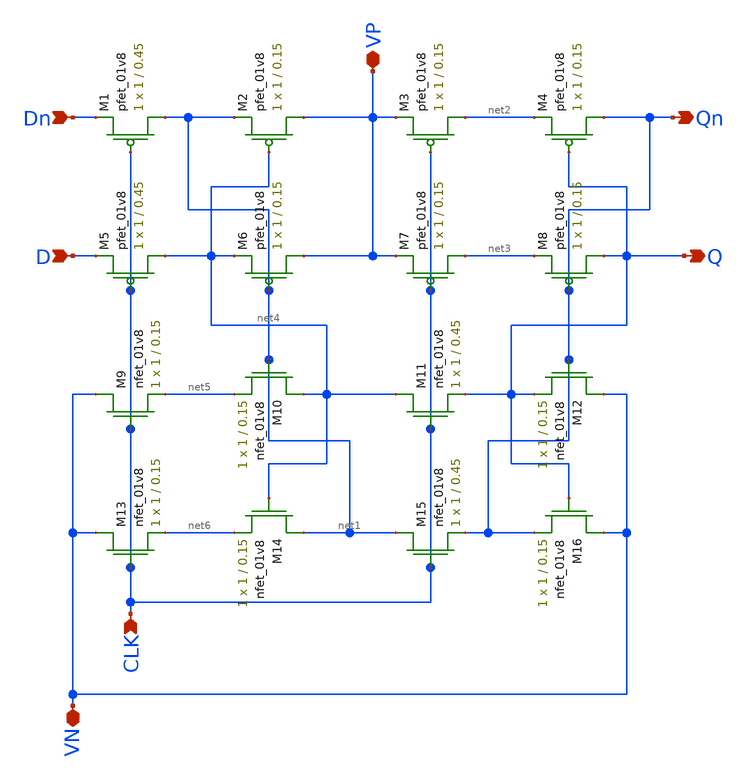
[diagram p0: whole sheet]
** sch_path: mp2/d_ff.sch
**.subckt d_ff D Dn CLK VN VP Qn Q
*.ipin D
*.ipin Dn
*.ipin CLK
*.iopin VN
*.iopin VP
*.opin Qn
*.opin Q
XM1 net1 CLK Dn VDD sky130_fd_pr__pfet_01v8 L=0.45 W=1 nf=1 ad='int((nf+1)/2) * W/nf * 0.29' as='int((nf+2)/2) * W/nf * 0.29'
+ pd='2*int((nf+1)/2) * (W/nf + 0.29)' ps='2*int((nf+2)/2) * (W/nf + 0.29)' nrd='0.29 / W' nrs='0.29 / W'
+ sa=0 sb=0 sd=0 mult=1 m=1
XM2 VP net4 net1 VDD sky130_fd_pr__pfet_01v8 L=0.15 W=1 nf=1 ad='int((nf+1)/2) * W/nf * 0.29' as='int((nf+2)/2) * W/nf * 0.29'
+ pd='2*int((nf+1)/2) * (W/nf + 0.29)' ps='2*int((nf+2)/2) * (W/nf + 0.29)' nrd='0.29 / W' nrs='0.29 / W'
+ sa=0 sb=0 sd=0 mult=1 m=1
XM3 net2 CLK VP VDD sky130_fd_pr__pfet_01v8 L=0.15 W=1 nf=1 ad='int((nf+1)/2) * W/nf * 0.29' as='int((nf+2)/2) * W/nf * 0.29'
+ pd='2*int((nf+1)/2) * (W/nf + 0.29)' ps='2*int((nf+2)/2) * (W/nf + 0.29)' nrd='0.29 / W' nrs='0.29 / W'
+ sa=0 sb=0 sd=0 mult=1 m=1
XM4 Qn Q net2 VDD sky130_fd_pr__pfet_01v8 L=0.15 W=1 nf=1 ad='int((nf+1)/2) * W/nf * 0.29' as='int((nf+2)/2) * W/nf * 0.29'
+ pd='2*int((nf+1)/2) * (W/nf + 0.29)' ps='2*int((nf+2)/2) * (W/nf + 0.29)' nrd='0.29 / W' nrs='0.29 / W'
+ sa=0 sb=0 sd=0 mult=1 m=1
XM5 net4 CLK D VDD sky130_fd_pr__pfet_01v8 L=0.45 W=1 nf=1 ad='int((nf+1)/2) * W/nf * 0.29' as='int((nf+2)/2) * W/nf * 0.29'
+ pd='2*int((nf+1)/2) * (W/nf + 0.29)' ps='2*int((nf+2)/2) * (W/nf + 0.29)' nrd='0.29 / W' nrs='0.29 / W'
+ sa=0 sb=0 sd=0 mult=1 m=1
XM6 VP net1 net4 VDD sky130_fd_pr__pfet_01v8 L=0.15 W=1 nf=1 ad='int((nf+1)/2) * W/nf * 0.29' as='int((nf+2)/2) * W/nf * 0.29'
+ pd='2*int((nf+1)/2) * (W/nf + 0.29)' ps='2*int((nf+2)/2) * (W/nf + 0.29)' nrd='0.29 / W' nrs='0.29 / W'
+ sa=0 sb=0 sd=0 mult=1 m=1
XM7 net3 CLK VP VDD sky130_fd_pr__pfet_01v8 L=0.15 W=1 nf=1 ad='int((nf+1)/2) * W/nf * 0.29' as='int((nf+2)/2) * W/nf * 0.29'
+ pd='2*int((nf+1)/2) * (W/nf + 0.29)' ps='2*int((nf+2)/2) * (W/nf + 0.29)' nrd='0.29 / W' nrs='0.29 / W'
+ sa=0 sb=0 sd=0 mult=1 m=1
XM8 Q Qn net3 VDD sky130_fd_pr__pfet_01v8 L=0.15 W=1 nf=1 ad='int((nf+1)/2) * W/nf * 0.29' as='int((nf+2)/2) * W/nf * 0.29'
+ pd='2*int((nf+1)/2) * (W/nf + 0.29)' ps='2*int((nf+2)/2) * (W/nf + 0.29)' nrd='0.29 / W' nrs='0.29 / W'
+ sa=0 sb=0 sd=0 mult=1 m=1
XM9 VN CLK net5 GND sky130_fd_pr__nfet_01v8 L=0.15 W=1 nf=1 ad='int((nf+1)/2) * W/nf * 0.29' as='int((nf+2)/2) * W/nf * 0.29'
+ pd='2*int((nf+1)/2) * (W/nf + 0.29)' ps='2*int((nf+2)/2) * (W/nf + 0.29)' nrd='0.29 / W' nrs='0.29 / W'
+ sa=0 sb=0 sd=0 mult=1 m=1
XM10 net4 net1 net5 GND sky130_fd_pr__nfet_01v8 L=0.15 W=1 nf=1 ad='int((nf+1)/2) * W/nf * 0.29' as='int((nf+2)/2) * W/nf * 0.29'
+ pd='2*int((nf+1)/2) * (W/nf + 0.29)' ps='2*int((nf+2)/2) * (W/nf + 0.29)' nrd='0.29 / W' nrs='0.29 / W'
+ sa=0 sb=0 sd=0 mult=1 m=1
XM11 net4 CLK Q GND sky130_fd_pr__nfet_01v8 L=0.45 W=1 nf=1 ad='int((nf+1)/2) * W/nf * 0.29' as='int((nf+2)/2) * W/nf * 0.29'
+ pd='2*int((nf+1)/2) * (W/nf + 0.29)' ps='2*int((nf+2)/2) * (W/nf + 0.29)' nrd='0.29 / W' nrs='0.29 / W'
+ sa=0 sb=0 sd=0 mult=1 m=1
XM12 VN Qn Q GND sky130_fd_pr__nfet_01v8 L=0.15 W=1 nf=1 ad='int((nf+1)/2) * W/nf * 0.29' as='int((nf+2)/2) * W/nf * 0.29'
+ pd='2*int((nf+1)/2) * (W/nf + 0.29)' ps='2*int((nf+2)/2) * (W/nf + 0.29)' nrd='0.29 / W' nrs='0.29 / W'
+ sa=0 sb=0 sd=0 mult=1 m=1
XM13 VN CLK net6 GND sky130_fd_pr__nfet_01v8 L=0.15 W=1 nf=1 ad='int((nf+1)/2) * W/nf * 0.29' as='int((nf+2)/2) * W/nf * 0.29'
+ pd='2*int((nf+1)/2) * (W/nf + 0.29)' ps='2*int((nf+2)/2) * (W/nf + 0.29)' nrd='0.29 / W' nrs='0.29 / W'
+ sa=0 sb=0 sd=0 mult=1 m=1
XM14 net1 net4 net6 GND sky130_fd_pr__nfet_01v8 L=0.15 W=1 nf=1 ad='int((nf+1)/2) * W/nf * 0.29' as='int((nf+2)/2) * W/nf * 0.29'
+ pd='2*int((nf+1)/2) * (W/nf + 0.29)' ps='2*int((nf+2)/2) * (W/nf + 0.29)' nrd='0.29 / W' nrs='0.29 / W'
+ sa=0 sb=0 sd=0 mult=1 m=1
XM15 net1 CLK Qn GND sky130_fd_pr__nfet_01v8 L=0.45 W=1 nf=1 ad='int((nf+1)/2) * W/nf * 0.29' as='int((nf+2)/2) * W/nf * 0.29'
+ pd='2*int((nf+1)/2) * (W/nf + 0.29)' ps='2*int((nf+2)/2) * (W/nf + 0.29)' nrd='0.29 / W' nrs='0.29 / W'
+ sa=0 sb=0 sd=0 mult=1 m=1
XM16 VN Q Qn GND sky130_fd_pr__nfet_01v8 L=0.15 W=1 nf=1 ad='int((nf+1)/2) * W/nf * 0.29' as='int((nf+2)/2) * W/nf * 0.29'
+ pd='2*int((nf+1)/2) * (W/nf + 0.29)' ps='2*int((nf+2)/2) * (W/nf + 0.29)' nrd='0.29 / W' nrs='0.29 / W'
+ sa=0 sb=0 sd=0 mult=1 m=1
**.ends
.end
